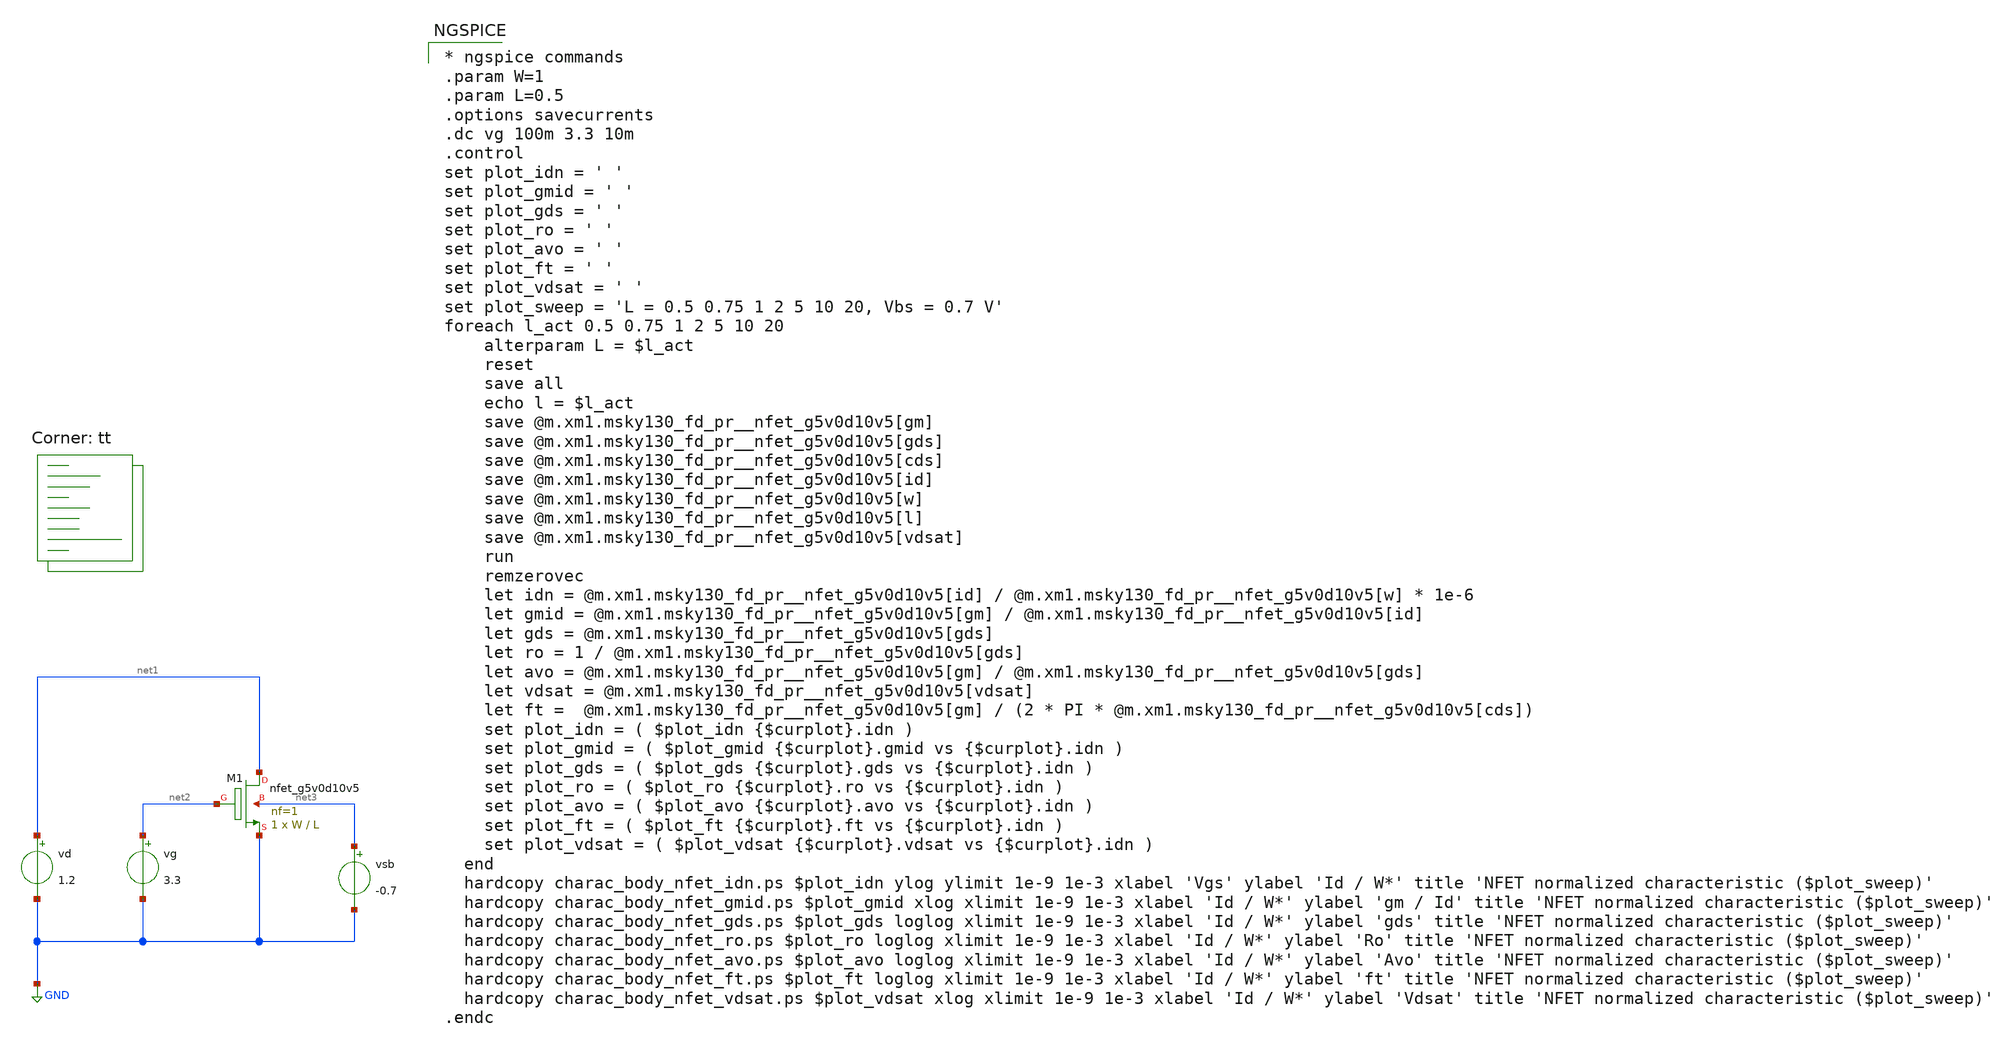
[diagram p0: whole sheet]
** sch_path: xschem/gmid_body_nfet_tb.sch
**.subckt gmid_body_nfet_tb
vd net1 GND 1.2
vg net2 GND 3.3
vsb net3 GND -0.7
XM1 net1 net2 GND net3 sky130_fd_pr__nfet_g5v0d10v5 L=L W=W nf=1 ad='int((nf+1)/2) * W/nf * 0.29' as='int((nf+2)/2) * W/nf * 0.29'
+ pd='2*int((nf+1)/2) * (W/nf + 0.29)' ps='2*int((nf+2)/2) * (W/nf + 0.29)' nrd='0.29 / W' nrs='0.29 / W'
+ sa=0 sb=0 sd=0 mult=1 m=1
**** begin user architecture code
.lib $::SKYWATER_MODELS/sky130.lib.spice tt

* ngspice commands
.param W=1
.param L=0.5
.options savecurrents
.dc vg 100m 3.3 10m
.control
set plot_idn = ' '
set plot_gmid = ' '
set plot_gds = ' '
set plot_ro = ' '
set plot_avo = ' '
set plot_ft = ' '
set plot_vdsat = ' '
set plot_sweep = 'L = 0.5 0.75 1 2 5 10 20, Vbs = 0.7 V'
foreach l_act 0.5 0.75 1 2 5 10 20
    alterparam L = $l_act
    reset
    save all
    echo l = $l_act
    save @m.xm1.msky130_fd_pr__nfet_g5v0d10v5[gm]
    save @m.xm1.msky130_fd_pr__nfet_g5v0d10v5[gds]
    save @m.xm1.msky130_fd_pr__nfet_g5v0d10v5[cds]
    save @m.xm1.msky130_fd_pr__nfet_g5v0d10v5[id]
    save @m.xm1.msky130_fd_pr__nfet_g5v0d10v5[w]
    save @m.xm1.msky130_fd_pr__nfet_g5v0d10v5[l]
    save @m.xm1.msky130_fd_pr__nfet_g5v0d10v5[vdsat]
    run
    remzerovec
    let idn = @m.xm1.msky130_fd_pr__nfet_g5v0d10v5[id] / @m.xm1.msky130_fd_pr__nfet_g5v0d10v5[w] *
+ 1e-6
    let gmid = @m.xm1.msky130_fd_pr__nfet_g5v0d10v5[gm] / @m.xm1.msky130_fd_pr__nfet_g5v0d10v5[id]
    let gds = @m.xm1.msky130_fd_pr__nfet_g5v0d10v5[gds]
    let ro = 1 / @m.xm1.msky130_fd_pr__nfet_g5v0d10v5[gds]
    let avo = @m.xm1.msky130_fd_pr__nfet_g5v0d10v5[gm] / @m.xm1.msky130_fd_pr__nfet_g5v0d10v5[gds]
    let vdsat = @m.xm1.msky130_fd_pr__nfet_g5v0d10v5[vdsat]
    let ft =  @m.xm1.msky130_fd_pr__nfet_g5v0d10v5[gm] / (2 * PI *
+ @m.xm1.msky130_fd_pr__nfet_g5v0d10v5[cds])
    set plot_idn = ( $plot_idn {$curplot}.idn )
    set plot_gmid = ( $plot_gmid {$curplot}.gmid vs {$curplot}.idn )
    set plot_gds = ( $plot_gds {$curplot}.gds vs {$curplot}.idn )
    set plot_ro = ( $plot_ro {$curplot}.ro vs {$curplot}.idn )
    set plot_avo = ( $plot_avo {$curplot}.avo vs {$curplot}.idn )
    set plot_ft = ( $plot_ft {$curplot}.ft vs {$curplot}.idn )
    set plot_vdsat = ( $plot_vdsat {$curplot}.vdsat vs {$curplot}.idn )
  end
  hardcopy charac_body_nfet_idn.ps $plot_idn ylog ylimit 1e-9 1e-3 xlabel 'Vgs' ylabel 'Id / W*' title
+ 'NFET normalized characteristic ($plot_sweep)'
  hardcopy charac_body_nfet_gmid.ps $plot_gmid xlog xlimit 1e-9 1e-3 xlabel 'Id / W*' ylabel 'gm / Id'
+ title 'NFET normalized characteristic ($plot_sweep)'
  hardcopy charac_body_nfet_gds.ps $plot_gds loglog xlimit 1e-9 1e-3 xlabel 'Id / W*' ylabel 'gds' title
+ 'NFET normalized characteristic ($plot_sweep)'
  hardcopy charac_body_nfet_ro.ps $plot_ro loglog xlimit 1e-9 1e-3 xlabel 'Id / W*' ylabel 'Ro' title
+ 'NFET normalized characteristic ($plot_sweep)'
  hardcopy charac_body_nfet_avo.ps $plot_avo loglog xlimit 1e-9 1e-3 xlabel 'Id / W*' ylabel 'Avo' title
+ 'NFET normalized characteristic ($plot_sweep)'
  hardcopy charac_body_nfet_ft.ps $plot_ft loglog xlimit 1e-9 1e-3 xlabel 'Id / W*' ylabel 'ft' title
+ 'NFET normalized characteristic ($plot_sweep)'
  hardcopy charac_body_nfet_vdsat.ps $plot_vdsat xlog xlimit 1e-9 1e-3 xlabel 'Id / W*' ylabel 'Vdsat'
+ title 'NFET normalized characteristic ($plot_sweep)'
.endc


**** end user architecture code
**.ends
.GLOBAL GND
.end
